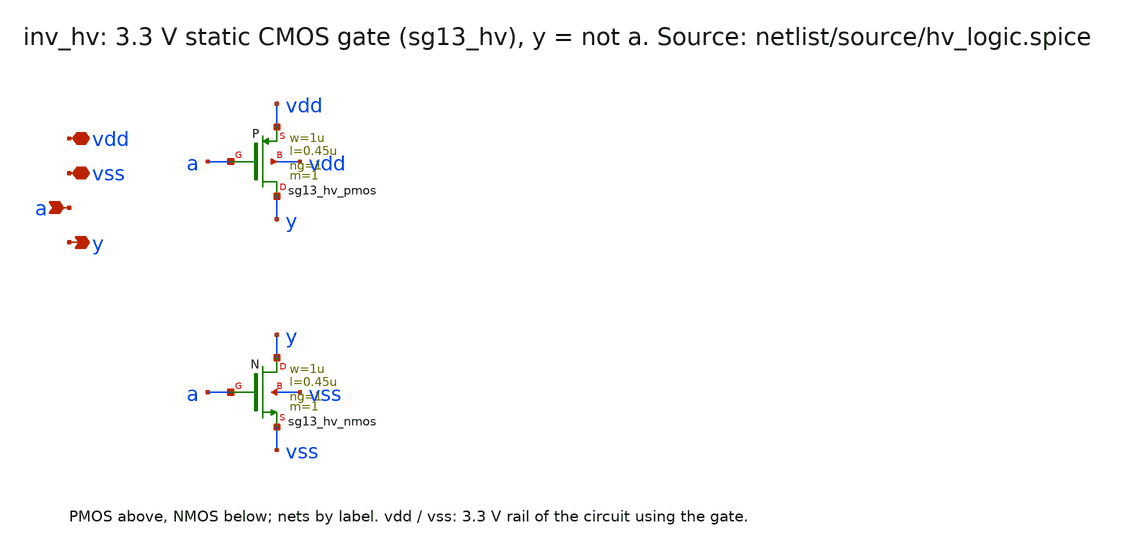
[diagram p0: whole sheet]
** sch_path: macros/hv_logic/schematic/xschem/inv_hv.sch
**.subckt inv_hv vdd vss a y
*.iopin vdd
*.iopin vss
*.ipin a
*.opin y
XP y a vdd vdd sg13_hv_pmos w=1u l=0.45u ng=1 m=1 mm_ok=1
XN y a vss vss sg13_hv_nmos w=1u l=0.45u ng=1 m=1 mm_ok=1
**.ends
.end
